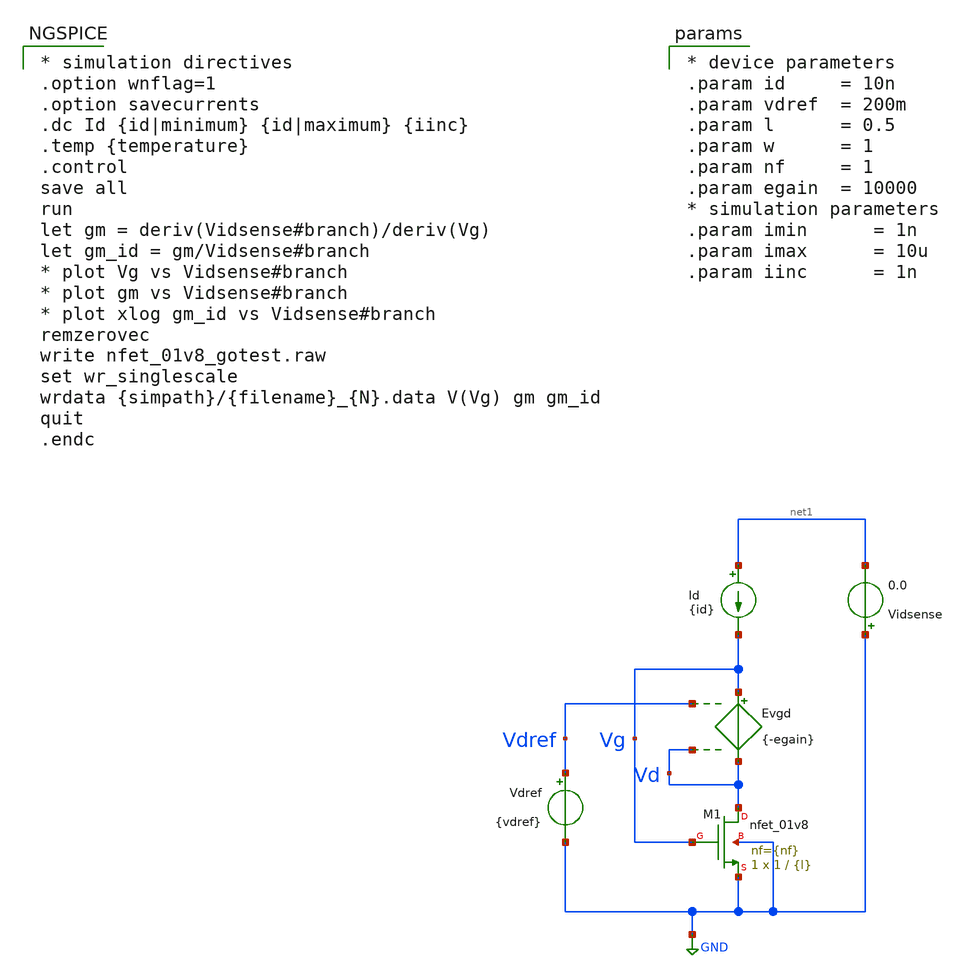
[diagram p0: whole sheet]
** sch_path: cace/tb_nfet_01v8_gmtest.sch
**.subckt tb_nfet_01v8_gmtest
Evgd Vg Vd Vdref Vd {-egain}
Id net1 Vg {id}
Vdref Vdref GND {vdref}
Vidsense GND net1 0.0
XM1 Vd Vg GND GND sky130_fd_pr__nfet_01v8 L={l} W=1 nf={nf} ad='int((nf+1)/2) * W/nf * 0.29' as='int((nf+2)/2) * W/nf * 0.29'
+ pd='2*int((nf+1)/2) * (W/nf + 0.29)' ps='2*int((nf+2)/2) * (W/nf + 0.29)' nrd='0.29 / W' nrs='0.29 / W'
+ sa=0 sb=0 sd=0 mult=1 m=1
**** begin user architecture code

** opencircuitdesign pdks install
.lib $::SKYWATER_MODELS/sky130.lib.spice {corner}



* simulation directives
.option wnflag=1
.option savecurrents
.dc Id {id|minimum} {id|maximum} {iinc}
.temp {temperature}
.control
save all
run
let gm = deriv(Vidsense#branch)/deriv(Vg)
let gm_id = gm/Vidsense#branch
* plot Vg vs Vidsense#branch
* plot gm vs Vidsense#branch
* plot xlog gm_id vs Vidsense#branch
remzerovec
write nfet_01v8_gotest.raw
set wr_singlescale
wrdata {simpath}/{filename}_{N}.data V(Vg) gm gm_id
quit
.endc



* device parameters
.param id     = 10n
.param vdref  = 200m
.param l      = 0.5
.param w      = 1
.param nf     = 1
.param egain  = 10000
* simulation parameters
.param imin      = 1n
.param imax      = 10u
.param iinc      = 1n


**** end user architecture code
**.ends
.GLOBAL GND
.end
